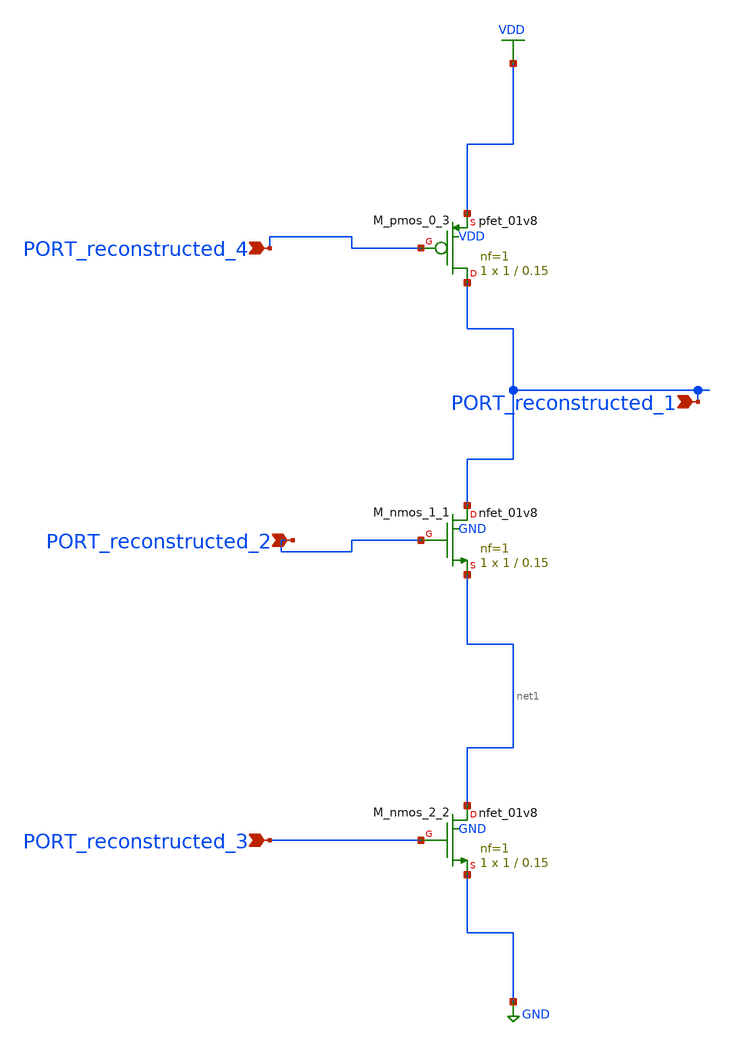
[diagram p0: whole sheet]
** sch_path: schematics/AMSNet/157.sch
**.subckt 157 PORT_reconstructed_2 PORT_reconstructed_3 PORT_reconstructed_4 PORT_reconstructed_1
*.ipin PORT_reconstructed_2
*.ipin PORT_reconstructed_3
*.ipin PORT_reconstructed_4
*.ipin PORT_reconstructed_1
XM_nmos_1_1 PORT_reconstructed_1 PORT_reconstructed_2 net1 GND sky130_fd_pr__nfet_01v8 L=0.15 W=1 nf=1
+ ad='int((1 + 1)/2) * 1 / 1 * 0.29' as='int((1 + 2)/2) * 1 / 1 * 0.29' pd='2*int((1 + 1)/2) * (1 / 1 + 0.29)'
+ ps='2*int((1 + 2)/2) * (1 / 1 + 0.29)' nrd='0.29 / 1 ' nrs='0.29 / 1 ' sa=0 sb=0 sd=0 mult=1 m=1
XM_nmos_2_2 net1 PORT_reconstructed_3 GND GND sky130_fd_pr__nfet_01v8 L=0.15 W=1 nf=1 ad='int((1 + 1)/2) * 1 / 1 * 0.29'
+ as='int((1 + 2)/2) * 1 / 1 * 0.29' pd='2*int((1 + 1)/2) * (1 / 1 + 0.29)' ps='2*int((1 + 2)/2) * (1 / 1 + 0.29)'
+ nrd='0.29 / 1 ' nrs='0.29 / 1 ' sa=0 sb=0 sd=0 mult=1 m=1
XM_pmos_0_3 PORT_reconstructed_1 PORT_reconstructed_4 VDD VDD sky130_fd_pr__pfet_01v8 L=0.15 W=1 nf=1
+ ad='int((1 + 1)/2) * 1 / 1 * 0.29' as='int((1 + 2)/2) * 1 / 1 * 0.29' pd='2*int((1 + 1)/2) * (1 / 1 + 0.29)'
+ ps='2*int((1 + 2)/2) * (1 / 1 + 0.29)' nrd='0.29 / 1 ' nrs='0.29 / 1 ' sa=0 sb=0 sd=0 mult=1 m=1
**.ends
.GLOBAL GND
.GLOBAL VDD
.end
